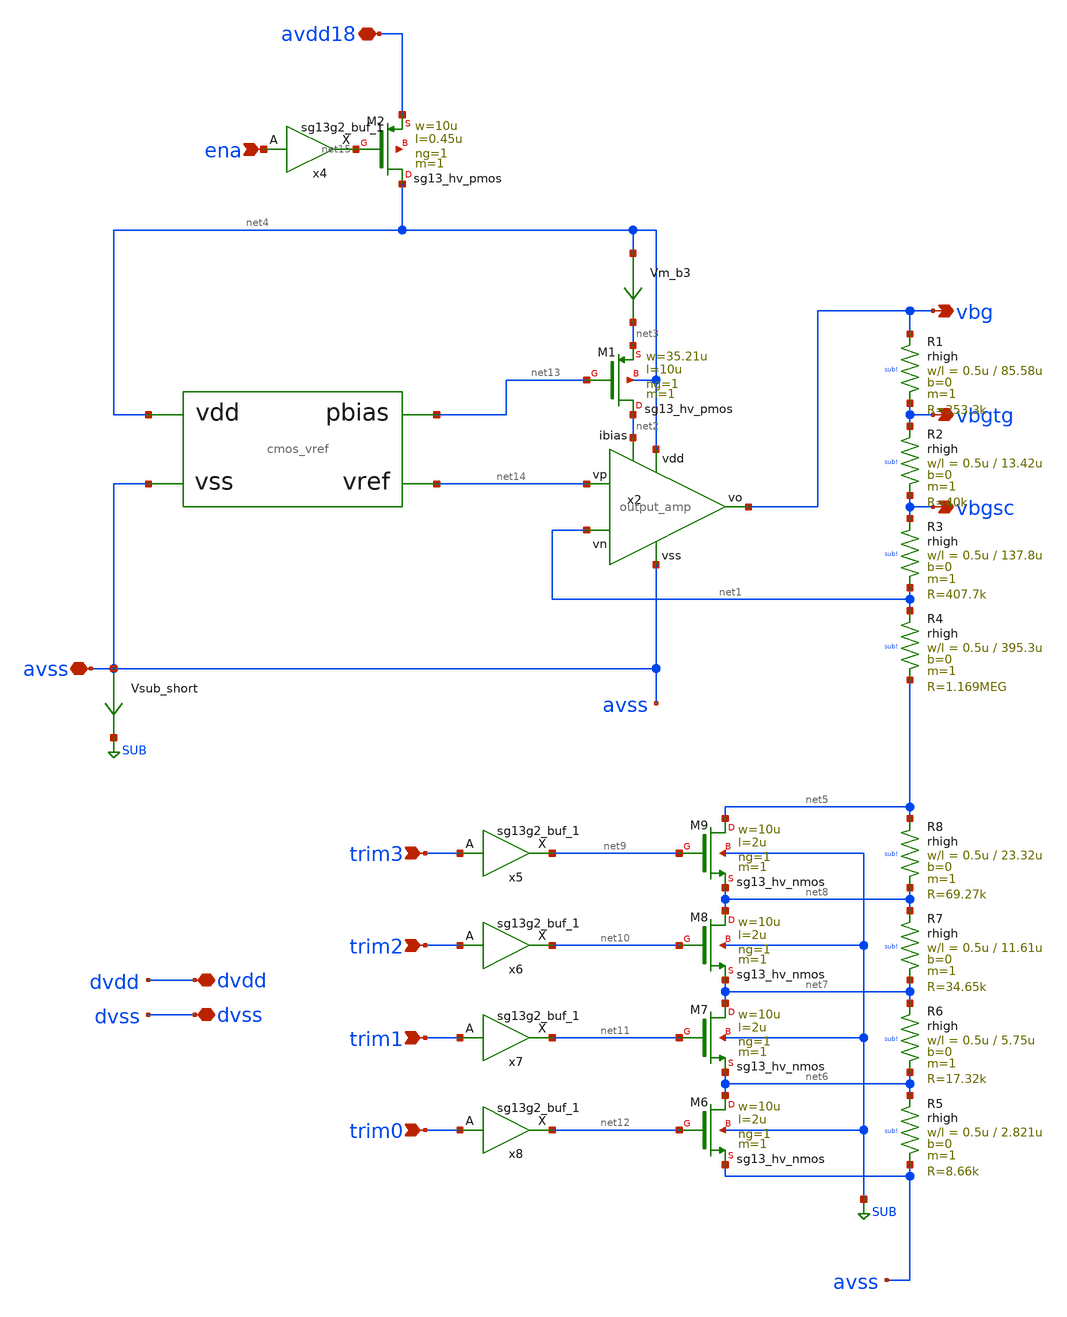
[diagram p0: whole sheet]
** sch_path: release/xschem/sch/top.sch
* IHP-GmbH/IHP-Open-PDK/ihp-sg13g2/libs.tech/xschem/sg13g2_stdcells/sg13g2_buf_1.sch:
* Copyright 2023 IHP PDK Authors
* Licensed under the Apache License, Version 2.0 (the "License");
**.subckt top vbg avss dvdd dvss vbgsc vbgtg trim3 trim2 trim1 trim0 avdd18 ena
*.opin vbg
*.iopin avss
*.iopin dvdd
*.iopin dvss
*.opin vbgsc
*.opin vbgtg
*.ipin trim3
*.ipin trim2
*.ipin trim1
*.ipin trim0
*.iopin avdd18
*.ipin ena
x2 net4 vbg net14 net1 net2 avss output_amp
Vm_b3 net4 net3 0
.save i(vm_b3)
Vsub_short avss SUB 0
.save i(vsub_short)
XM1 net2 net13 net3 net4 sg13_hv_pmos w=35.21u l=10u ng=1 m=1 mm_ok=1
x5 net9 trim3 VDD VSS sg13g2_buf_1
x6 net10 trim2 VDD VSS sg13g2_buf_1
x7 net11 trim1 VDD VSS sg13g2_buf_1
x8 net12 trim0 VDD VSS sg13g2_buf_1
XR1 vbg vbgtg sub! rhigh w=0.5u l=85.58u m=1 b=0 mm_ok=1
XR2 vbgtg vbgsc sub! rhigh w=0.5u l=13.42u m=1 b=0 mm_ok=1
XR3 vbgsc net1 sub! rhigh w=0.5u l=137.8u m=1 b=0 mm_ok=1
XR4 net1 net5 sub! rhigh w=0.5u l=395.3u m=1 b=0 mm_ok=1
XM6 net6 net12 avss SUB sg13_hv_nmos w=10u l=2u ng=1 m=1 mm_ok=1
XM7 net7 net11 net6 SUB sg13_hv_nmos w=10u l=2u ng=1 m=1 mm_ok=1
XM8 net8 net10 net7 SUB sg13_hv_nmos w=10u l=2u ng=1 m=1 mm_ok=1
XM9 net5 net9 net8 SUB sg13_hv_nmos w=10u l=2u ng=1 m=1 mm_ok=1
XR5 net6 avss sub! rhigh w=0.5u l=2.821u m=1 b=0 mm_ok=1
XR6 net7 net6 sub! rhigh w=0.5u l=5.75u m=1 b=0 mm_ok=1
XR7 net8 net7 sub! rhigh w=0.5u l=11.61u m=1 b=0 mm_ok=1
XR8 net5 net8 sub! rhigh w=0.5u l=23.32u m=1 b=0 mm_ok=1
X1 net14 net4 avss net13 cmos_vref
x4 net15 ena VDD VSS sg13g2_buf_1
XM2 net4 net15 avdd18 net16 sg13_hv_pmos w=10u l=0.45u ng=1 m=1 mm_ok=1
**.ends

* expanding   symbol:  sch/output_amp.sym # of pins=6
** sym_path: release/xschem/sch/output_amp.sym
** sch_path: release/xschem/sch/output_amp.sch
.subckt output_amp vdd vo vp vn ibias vss
*.ipin vp
*.ipin vn
*.ipin ibias
*.opin vo
*.ipin vss
*.ipin vdd
Vm_b1 vdd net3 0
.save i(vm_b1)
Vm_op vdd net5 0
.save i(vm_op)
Vm_cm vcm net2 0
.save i(vm_cm)
Vm_b2 vdd net4 0
.save i(vm_b2)
Vm_on vo net6 0
.save i(vm_on)
XM1 ibias ibias vss SUB sg13_hv_nmos w=2.5u l=1u ng=1 m=1 mm_ok=1
XM2 net2 ibias vss SUB sg13_hv_nmos w=5u l=1u ng=1 m=1 mm_ok=1
XM3 net6 ibias vss SUB sg13_hv_nmos w=8u l=1u ng=1 m=1 mm_ok=1
XM4 net7 vn vcm SUB sg13_hv_nmos w=10u l=2u ng=1 m=1 mm_ok=1
XM5 net8 vp vcm SUB sg13_hv_nmos w=10u l=2u ng=1 m=1 mm_ok=1
XC1 vo vo_pre cap_cmim w=5u l=5u m=1 mm_ok=1
XM6 net1 vn net7 SUB sg13_hv_nmos w=20u l=2u ng=1 m=1 mm_ok=1
XM7 vo_pre vp net8 SUB sg13_hv_nmos w=20u l=2u ng=1 m=1 mm_ok=1
XM8 net1 net1 net3 vdd sg13_hv_pmos w=5u l=10u ng=1 m=1 mm_ok=1
XM9 vo_pre net1 net4 vdd sg13_hv_pmos w=5u l=10u ng=1 m=1 mm_ok=1
XM10 vo vo_pre net5 vdd sg13_hv_pmos w=40u l=5u ng=1 m=1 mm_ok=1
.ends


* expanding   symbol:  sg13g2_stdcells/sg13g2_buf_1.sym # of pins=2
** sym_path: sg13g2_stdcells/sg13g2_buf_1.sym
** sch_path: sg13g2_stdcells/sg13g2_buf_1.sch
.subckt sg13g2_buf_1 X A VDD VSS
*.ipin A
*.opin X
*.iopin VDD
*.iopin VSS
XM1 net1 A VSS VSS sg13_lv_nmos w=550.00n l=130.00n ng=1 m=1 mm_ok=1
XM2 X net1 VSS VSS sg13_lv_nmos w=740.00n l=130.00n ng=1 m=1 mm_ok=1
XM3 net1 A VDD VDD sg13_lv_pmos w=840.00n l=130.00n ng=1 m=1 mm_ok=1
XM4 X net1 VDD VDD sg13_lv_pmos w=1.12u l=130.00n ng=1 m=1 mm_ok=1
.ends


* expanding   symbol:  sch/cmos_vref.sym # of pins=4
** sym_path: release/xschem/sch/cmos_vref.sym
** sch_path: release/xschem/sch/cmos_vref.sch
.subckt cmos_vref vref vdd vss pbias
*.iopin vss
*.iopin vdd
*.opin pbias
*.opin vref
Vm_b1 vdd net1 0
.save i(vm_b1)
XM1 vptat vref vss vss sg13_hv_nmos w=2.5u l=20u ng=1 m=1 mm_ok=1
XM2 vref vref vptat vss sg13_hv_nmos w=2u l=10u ng=1 m=1 mm_ok=1
XM3 vref pbias net1 vdd sg13_hv_pmos w=50u l=10u ng=1 m=1 mm_ok=1
Vm_st1 pbias net5 0
.save i(vm_st1)
Vm_st2 vdd net6 0
.save i(vm_st2)
Vm_b3 vdd net7 0
.save i(vm_b3)
Vm_b4 vdd net8 0
.save i(vm_b4)
XM7 net3 vbias_st vss vss sg13_hv_nmos w=5u l=2u ng=1 m=1 mm_ok=1
XM11 vbias_st pbias net8 vdd sg13_hv_pmos w=5u l=10u ng=1 m=1 mm_ok=1
XM6 net2 vbias_st vptat vss sg13_hv_nmos w=100u l=2u ng=1 m=1 mm_ok=1
XM9 vbias_st vref net3 vss sg13_hv_nmos w=10u l=10u ng=1 m=1 mm_ok=1
XM8 pbias vref net2 vss sg13_hv_nmos w=10u l=10u ng=1 m=1 mm_ok=1
XM10 pbias pbias net7 vdd sg13_hv_pmos w=5u l=10u ng=1 m=1 mm_ok=1
XM13 net4 vbias_st vss vss sg13_hv_nmos w=10u l=5u ng=1 m=1 mm_ok=1
XM12 net5 net4 vss vss sg13_hv_nmos w=5u l=10u ng=1 m=1 mm_ok=1
XC1 net6 net4 cap_cmim w=7u l=7u m=10 mm_ok=1
.ends

.GLOBAL SUB
.end
